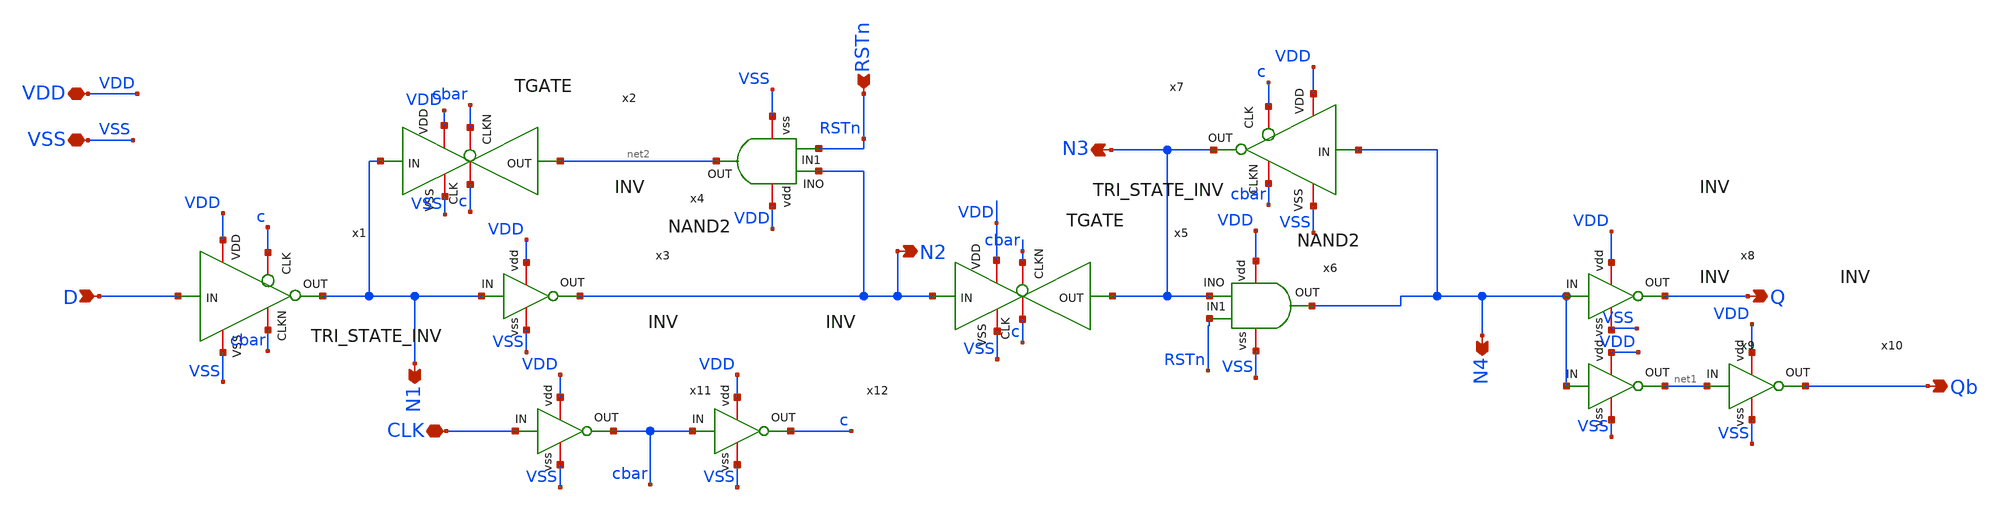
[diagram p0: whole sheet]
** sch_path: CAD6/DFF_Ray/old_DFF.sch
**.subckt old_DFF D RSTn Q Qb CLK VDD VSS N1 N2 N3 N4
*.ipin D
*.ipin RSTn
*.opin Q
*.opin Qb
*.iopin CLK
*.iopin VDD
*.iopin VSS
*.opin N1
*.opin N2
*.opin N3
*.opin N4
x2 c VDD VSS N1 net2 cbar TGATE
x3 VDD N1 N2 VSS INV
x4 VDD N2 net2 RSTn VSS NAND2
x5 c VDD VSS N2 N3 cbar TGATE
x6 VDD N3 N4 RSTn VSS NAND2
x1 VDD c N1 D cbar VSS TRI_STATE_INV
x7 VDD c N3 N4 cbar VSS TRI_STATE_INV
x8 VDD N4 Q net3 INV
x9 VDD N4 net1 VSS INV
x10 VDD net1 Qb VSS INV
x11 VDD CLK cbar VSS INV
x12 VDD cbar c VSS INV
**.ends

* expanding   symbol:  CAD2/TGATE.sym # of pins=6
** sym_path: CAD6/DFF_Ray/TGATE.sym
** sch_path: CAD6/DFF_Ray/TGATE.sch
.subckt TGATE CLK VDD VSS IN OUT CLKN
*.ipin IN
*.opin OUT
*.iopin CLKN
*.iopin CLK
*.iopin VDD
*.iopin VSS
XM1 IN CLK OUT VSS nfet_03v3 L=0.28u W=1u nf=1 ad='int((nf+1)/2) * W/nf * 0.18u' as='int((nf+2)/2) * W/nf * 0.18u'
+ pd='2*int((nf+1)/2) * (W/nf + 0.18u)' ps='2*int((nf+2)/2) * (W/nf + 0.18u)' nrd='0.18u / W' nrs='0.18u / W'
+ sa=0 sb=0 sd=0 m=1
XM2 IN CLKN OUT VDD pfet_03v3 L=0.28u W=2u nf=1 ad='int((nf+1)/2) * W/nf * 0.18u' as='int((nf+2)/2) * W/nf * 0.18u'
+ pd='2*int((nf+1)/2) * (W/nf + 0.18u)' ps='2*int((nf+2)/2) * (W/nf + 0.18u)' nrd='0.18u / W' nrs='0.18u / W'
+ sa=0 sb=0 sd=0 m=1
.ends


* expanding   symbol:  CAD2/INV.sym # of pins=4
** sym_path: CAD6/DFF_Ray/INV.sym
** sch_path: CAD6/DFF_Ray/INV.sch
.subckt INV vdd IN OUT vss
*.ipin IN
*.opin OUT
*.iopin vss
*.iopin vdd
XM1 OUT IN vss vss nfet_03v3 L=0.28u W=1u nf=1 ad='int((nf+1)/2) * W/nf * 0.18u' as='int((nf+2)/2) * W/nf * 0.18u'
+ pd='2*int((nf+1)/2) * (W/nf + 0.18u)' ps='2*int((nf+2)/2) * (W/nf + 0.18u)' nrd='0.18u / W' nrs='0.18u / W'
+ sa=0 sb=0 sd=0 m=1
XM2 OUT IN vdd vdd pfet_03v3 L=0.28u W=2u nf=1 ad='int((nf+1)/2) * W/nf * 0.18u' as='int((nf+2)/2) * W/nf * 0.18u'
+ pd='2*int((nf+1)/2) * (W/nf + 0.18u)' ps='2*int((nf+2)/2) * (W/nf + 0.18u)' nrd='0.18u / W' nrs='0.18u / W'
+ sa=0 sb=0 sd=0 m=1
.ends


* expanding   symbol:  CAD2/NAND2.sym # of pins=5
** sym_path: CAD6/DFF_Ray/NAND2.sym
** sch_path: CAD6/DFF_Ray/NAND2.sch
.subckt NAND2 vdd INO OUT IN1 vss
*.ipin INO
*.ipin IN1
*.iopin vdd
*.iopin vss
*.opin OUT
XM1 OUT INO net1 vss nfet_03v3 L=0.28u W=2u nf=1 ad='int((nf+1)/2) * W/nf * 0.18u' as='int((nf+2)/2) * W/nf * 0.18u'
+ pd='2*int((nf+1)/2) * (W/nf + 0.18u)' ps='2*int((nf+2)/2) * (W/nf + 0.18u)' nrd='0.18u / W' nrs='0.18u / W'
+ sa=0 sb=0 sd=0 m=1
XM2 net1 IN1 vss vss nfet_03v3 L=0.28u W=2u nf=1 ad='int((nf+1)/2) * W/nf * 0.18u' as='int((nf+2)/2) * W/nf * 0.18u'
+ pd='2*int((nf+1)/2) * (W/nf + 0.18u)' ps='2*int((nf+2)/2) * (W/nf + 0.18u)' nrd='0.18u / W' nrs='0.18u / W'
+ sa=0 sb=0 sd=0 m=1
XM3 OUT INO vdd vdd pfet_03v3 L=0.28u W=2u nf=1 ad='int((nf+1)/2) * W/nf * 0.18u' as='int((nf+2)/2) * W/nf * 0.18u'
+ pd='2*int((nf+1)/2) * (W/nf + 0.18u)' ps='2*int((nf+2)/2) * (W/nf + 0.18u)' nrd='0.18u / W' nrs='0.18u / W'
+ sa=0 sb=0 sd=0 m=1
XM4 OUT IN1 vdd vdd pfet_03v3 L=0.28u W=2u nf=1 ad='int((nf+1)/2) * W/nf * 0.18u' as='int((nf+2)/2) * W/nf * 0.18u'
+ pd='2*int((nf+1)/2) * (W/nf + 0.18u)' ps='2*int((nf+2)/2) * (W/nf + 0.18u)' nrd='0.18u / W' nrs='0.18u / W'
+ sa=0 sb=0 sd=0 m=1
.ends


* expanding   symbol:  CAD2/TRI_STATE_INV.sym # of pins=6
** sym_path: CAD6/DFF_Ray/TRI_STATE_INV.sym
** sch_path: CAD6/DFF_Ray/TRI_STATE_INV.sch
.subckt TRI_STATE_INV VDD CLK OUT IN CLKN VSS
*.iopin VSS
*.iopin VDD
*.iopin CLK
*.iopin CLKN
*.ipin IN
*.opin OUT
XM1 net1 CLK VDD VDD pfet_03v3 L=0.28u W=4u nf=1 ad='int((nf+1)/2) * W/nf * 0.18u' as='int((nf+2)/2) * W/nf * 0.18u'
+ pd='2*int((nf+1)/2) * (W/nf + 0.18u)' ps='2*int((nf+2)/2) * (W/nf + 0.18u)' nrd='0.18u / W' nrs='0.18u / W'
+ sa=0 sb=0 sd=0 m=1
XM2 OUT IN net1 VDD pfet_03v3 L=0.28u W=4u nf=1 ad='int((nf+1)/2) * W/nf * 0.18u' as='int((nf+2)/2) * W/nf * 0.18u'
+ pd='2*int((nf+1)/2) * (W/nf + 0.18u)' ps='2*int((nf+2)/2) * (W/nf + 0.18u)' nrd='0.18u / W' nrs='0.18u / W'
+ sa=0 sb=0 sd=0 m=1
XM3 OUT IN net2 VSS nfet_03v3 L=0.28u W=2u nf=1 ad='int((nf+1)/2) * W/nf * 0.18u' as='int((nf+2)/2) * W/nf * 0.18u'
+ pd='2*int((nf+1)/2) * (W/nf + 0.18u)' ps='2*int((nf+2)/2) * (W/nf + 0.18u)' nrd='0.18u / W' nrs='0.18u / W'
+ sa=0 sb=0 sd=0 m=1
XM4 net2 CLKN VSS VSS nfet_03v3 L=0.28u W=2u nf=1 ad='int((nf+1)/2) * W/nf * 0.18u' as='int((nf+2)/2) * W/nf * 0.18u'
+ pd='2*int((nf+1)/2) * (W/nf + 0.18u)' ps='2*int((nf+2)/2) * (W/nf + 0.18u)' nrd='0.18u / W' nrs='0.18u / W'
+ sa=0 sb=0 sd=0 m=1
.ends

.end
